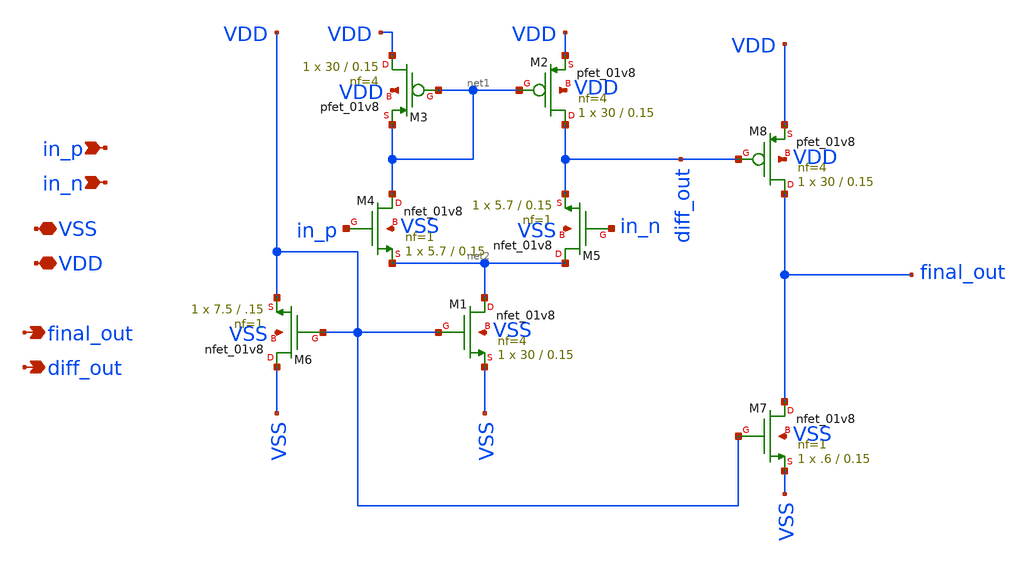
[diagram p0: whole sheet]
** sch_path: xschem/src/amplifier.sch
**.subckt amplifier in_p VDD in_n VSS final_out diff_out
*.ipin in_p
*.iopin VDD
*.ipin in_n
*.iopin VSS
*.opin final_out
*.opin diff_out
XM1 net2 VDD VSS VSS sky130_fd_pr__nfet_01v8 L=0.15 W=30 nf=4 ad='int((nf+1)/2) * W/nf * 0.29' as='int((nf+2)/2) * W/nf * 0.29'
+ pd='2*int((nf+1)/2) * (W/nf + 0.29)' ps='2*int((nf+2)/2) * (W/nf + 0.29)' nrd='0.29 / W' nrs='0.29 / W'
+ sa=0 sb=0 sd=0 mult=1 m=1
XM2 diff_out net1 VDD VDD sky130_fd_pr__pfet_01v8 L=0.15 W=30 nf=4 ad='int((nf+1)/2) * W/nf * 0.29' as='int((nf+2)/2) * W/nf * 0.29'
+ pd='2*int((nf+1)/2) * (W/nf + 0.29)' ps='2*int((nf+2)/2) * (W/nf + 0.29)' nrd='0.29 / W' nrs='0.29 / W'
+ sa=0 sb=0 sd=0 mult=1 m=1
XM3 VDD net1 net1 VDD sky130_fd_pr__pfet_01v8 L=0.15 W=30 nf=4 ad='int((nf+1)/2) * W/nf * 0.29' as='int((nf+2)/2) * W/nf * 0.29'
+ pd='2*int((nf+1)/2) * (W/nf + 0.29)' ps='2*int((nf+2)/2) * (W/nf + 0.29)' nrd='0.29 / W' nrs='0.29 / W'
+ sa=0 sb=0 sd=0 mult=1 m=1
XM4 net1 in_p net2 VSS sky130_fd_pr__nfet_01v8 L=0.15 W=5.7 nf=1 ad='int((nf+1)/2) * W/nf * 0.29' as='int((nf+2)/2) * W/nf * 0.29'
+ pd='2*int((nf+1)/2) * (W/nf + 0.29)' ps='2*int((nf+2)/2) * (W/nf + 0.29)' nrd='0.29 / W' nrs='0.29 / W'
+ sa=0 sb=0 sd=0 mult=1 m=1
XM5 net2 in_n diff_out VSS sky130_fd_pr__nfet_01v8 L=0.15 W=5.7 nf=1 ad='int((nf+1)/2) * W/nf * 0.29'
+ as='int((nf+2)/2) * W/nf * 0.29' pd='2*int((nf+1)/2) * (W/nf + 0.29)' ps='2*int((nf+2)/2) * (W/nf + 0.29)'
+ nrd='0.29 / W' nrs='0.29 / W' sa=0 sb=0 sd=0 mult=1 m=1
XM6 VSS VDD VDD VSS sky130_fd_pr__nfet_01v8 L=.15 W=7.5 nf=1 ad='int((nf+1)/2) * W/nf * 0.29' as='int((nf+2)/2) * W/nf * 0.29'
+ pd='2*int((nf+1)/2) * (W/nf + 0.29)' ps='2*int((nf+2)/2) * (W/nf + 0.29)' nrd='0.29 / W' nrs='0.29 / W'
+ sa=0 sb=0 sd=0 mult=1 m=1
XM7 final_out VDD VSS VSS sky130_fd_pr__nfet_01v8 L=0.15 W=.6 nf=1 ad='int((nf+1)/2) * W/nf * 0.29' as='int((nf+2)/2) * W/nf * 0.29'
+ pd='2*int((nf+1)/2) * (W/nf + 0.29)' ps='2*int((nf+2)/2) * (W/nf + 0.29)' nrd='0.29 / W' nrs='0.29 / W'
+ sa=0 sb=0 sd=0 mult=1 m=1
XM8 final_out diff_out VDD VDD sky130_fd_pr__pfet_01v8 L=0.15 W=30 nf=4 ad='int((nf+1)/2) * W/nf * 0.29'
+ as='int((nf+2)/2) * W/nf * 0.29' pd='2*int((nf+1)/2) * (W/nf + 0.29)' ps='2*int((nf+2)/2) * (W/nf + 0.29)'
+ nrd='0.29 / W' nrs='0.29 / W' sa=0 sb=0 sd=0 mult=1 m=1
**.ends
.end
